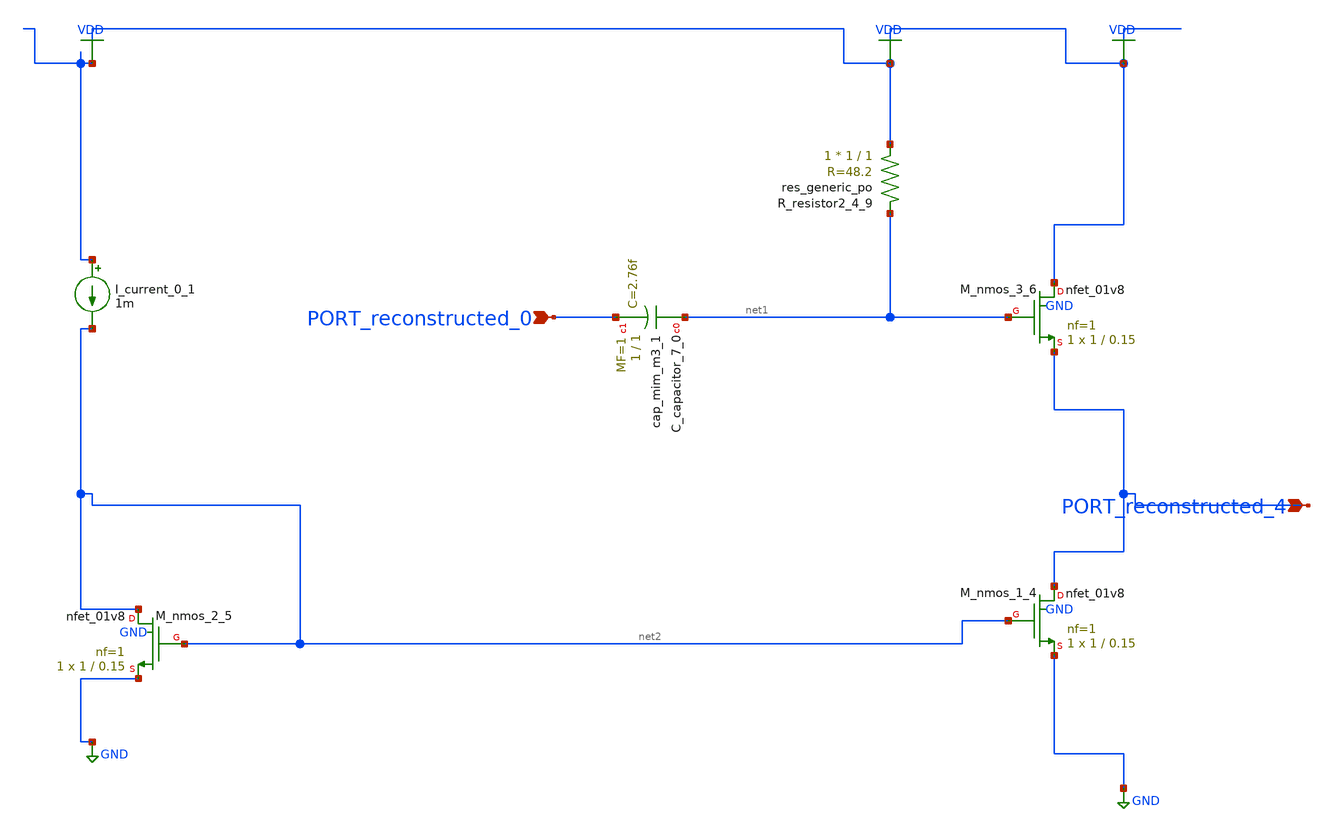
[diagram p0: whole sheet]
** sch_path: schematics/AMSNet/316.sch
**.subckt 316 PORT_reconstructed_4 PORT_reconstructed_0
*.ipin PORT_reconstructed_4
*.ipin PORT_reconstructed_0
XC_capacitor_7_0 net1 PORT_reconstructed_0 sky130_fd_pr__cap_mim_m3_1 W=1 L=1 MF=1 m=1
I_current_0_1 VDD net2 1m
XM_nmos_1_4 PORT_reconstructed_4 net2 GND GND sky130_fd_pr__nfet_01v8 L=0.15 W=1 nf=1 ad='int((1 + 1)/2) * 1 / 1 * 0.29'
+ as='int((1 + 2)/2) * 1 / 1 * 0.29' pd='2*int((1 + 1)/2) * (1 / 1 + 0.29)' ps='2*int((1 + 2)/2) * (1 / 1 + 0.29)'
+ nrd='0.29 / 1 ' nrs='0.29 / 1 ' sa=0 sb=0 sd=0 mult=1 m=1
XM_nmos_2_5 net2 net2 GND GND sky130_fd_pr__nfet_01v8 L=0.15 W=1 nf=1 ad='int((1 + 1)/2) * 1 / 1 * 0.29'
+ as='int((1 + 2)/2) * 1 / 1 * 0.29' pd='2*int((1 + 1)/2) * (1 / 1 + 0.29)' ps='2*int((1 + 2)/2) * (1 / 1 + 0.29)'
+ nrd='0.29 / 1 ' nrs='0.29 / 1 ' sa=0 sb=0 sd=0 mult=1 m=1
XM_nmos_3_6 VDD net1 PORT_reconstructed_4 GND sky130_fd_pr__nfet_01v8 L=0.15 W=1 nf=1 ad='int((1 + 1)/2) * 1 / 1 * 0.29'
+ as='int((1 + 2)/2) * 1 / 1 * 0.29' pd='2*int((1 + 1)/2) * (1 / 1 + 0.29)' ps='2*int((1 + 2)/2) * (1 / 1 + 0.29)'
+ nrd='0.29 / 1 ' nrs='0.29 / 1 ' sa=0 sb=0 sd=0 mult=1 m=1
XR_resistor2_4_9 VDD net1 sky130_fd_pr__res_generic_po W=1 L=1 m=1
**.ends
.GLOBAL GND
.GLOBAL VDD
.end
